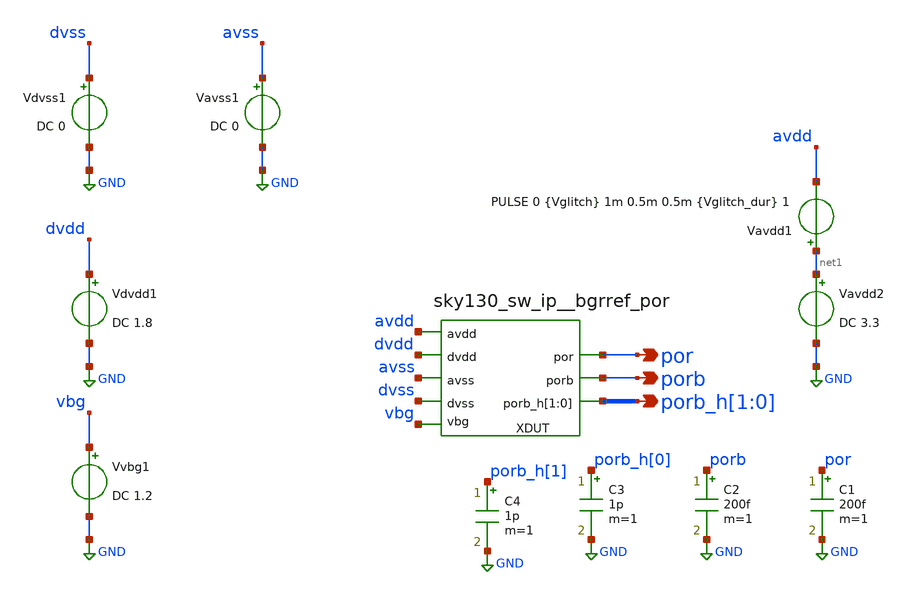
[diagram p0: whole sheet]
** sch_path: cace/templates/temp/por_supply_glitch_temp.sch
**.subckt por_supply_glitch_temp por porb porb_h[1],porb_h[0]
*.opin por
*.opin porb
*.opin porb_h[1],porb_h[0]
XDUT vbg por avss avdd dvdd porb dvss porb_h[1] porb_h[0] sky130_sw_ip__bgrref_por
C1 por GND 200f m=1
C2 porb GND 200f m=1
C3 porb_h[0] GND 1p m=1
C4 porb_h[1] GND 1p m=1
Vavdd1 net1 avdd PULSE 0 {Vglitch} 1m 0.5m 0.5m {Vglitch_dur} 1
Vavdd2 net1 GND DC 3.3
Vdvss1 dvss GND DC 0
Vavss1 avss GND DC 0
Vdvdd1 dvdd GND DC 1.8
Vvbg1 vbg GND DC 1.2
**** begin user architecture code
 .lib $::SKYWATER_MODELS/../combined/sky130.lib.spice tt

.include $::SKYWATER_STDCELLS/sky130_fd_sc_hd.spice
.include $::SKYWATER_STDCELLS/../../sky130_fd_sc_hvl/spice/sky130_fd_sc_hvl.spice
.include $::SKYWATER_STDCELLS/../../sky130_fd_sc_ls/spice/sky130_fd_sc_ls.spice



.param Vglitch = 3.3
.param Vglitch_dur = 4m

.tran 0.1u 4m

.control
let dvdd_half = 0.5*1.8
* glitch duration sweep loop
let stop_dur = 200u
let delta_dur = 5u
let dur_act = 10u
let stop_amp = 3.3
let delta_amp = 100m
let amp_act = 3.1
while dur_act le stop_dur
 alterparam Vglitch_dur = $&dur_act
 reset
 run
 meas tran por_val FIND v(por) AT = 4m
 if por_val > dvdd_half
   echo $&dur_act  > ~/POR.data
   let dur_act = dur_act + stop_dur
   * glitch amplitude sweep loop
   while amp_act le stop_amp
     alterparam Vglitch = $&amp_act
     reset
     run
     meas tran por_val FIND v(por) AT = 4m
     if por_val > dvdd_half
       echo $&amp_act  >> ~/POR.data
       let amp_act = amp_act + stop_amp
     else
       let amp_act = amp_act + delta_amp
     end
   end
 else
   let dur_act = dur_act + delta_dur
 end
end


*quit

write sky130_sw_ip__bgrref_por_tb1.raw
* *wrdata  ~/POR_tran_array.data v(avdd) v(por)
 .endc


**** end user architecture code
**.ends
.GLOBAL GND
.end
